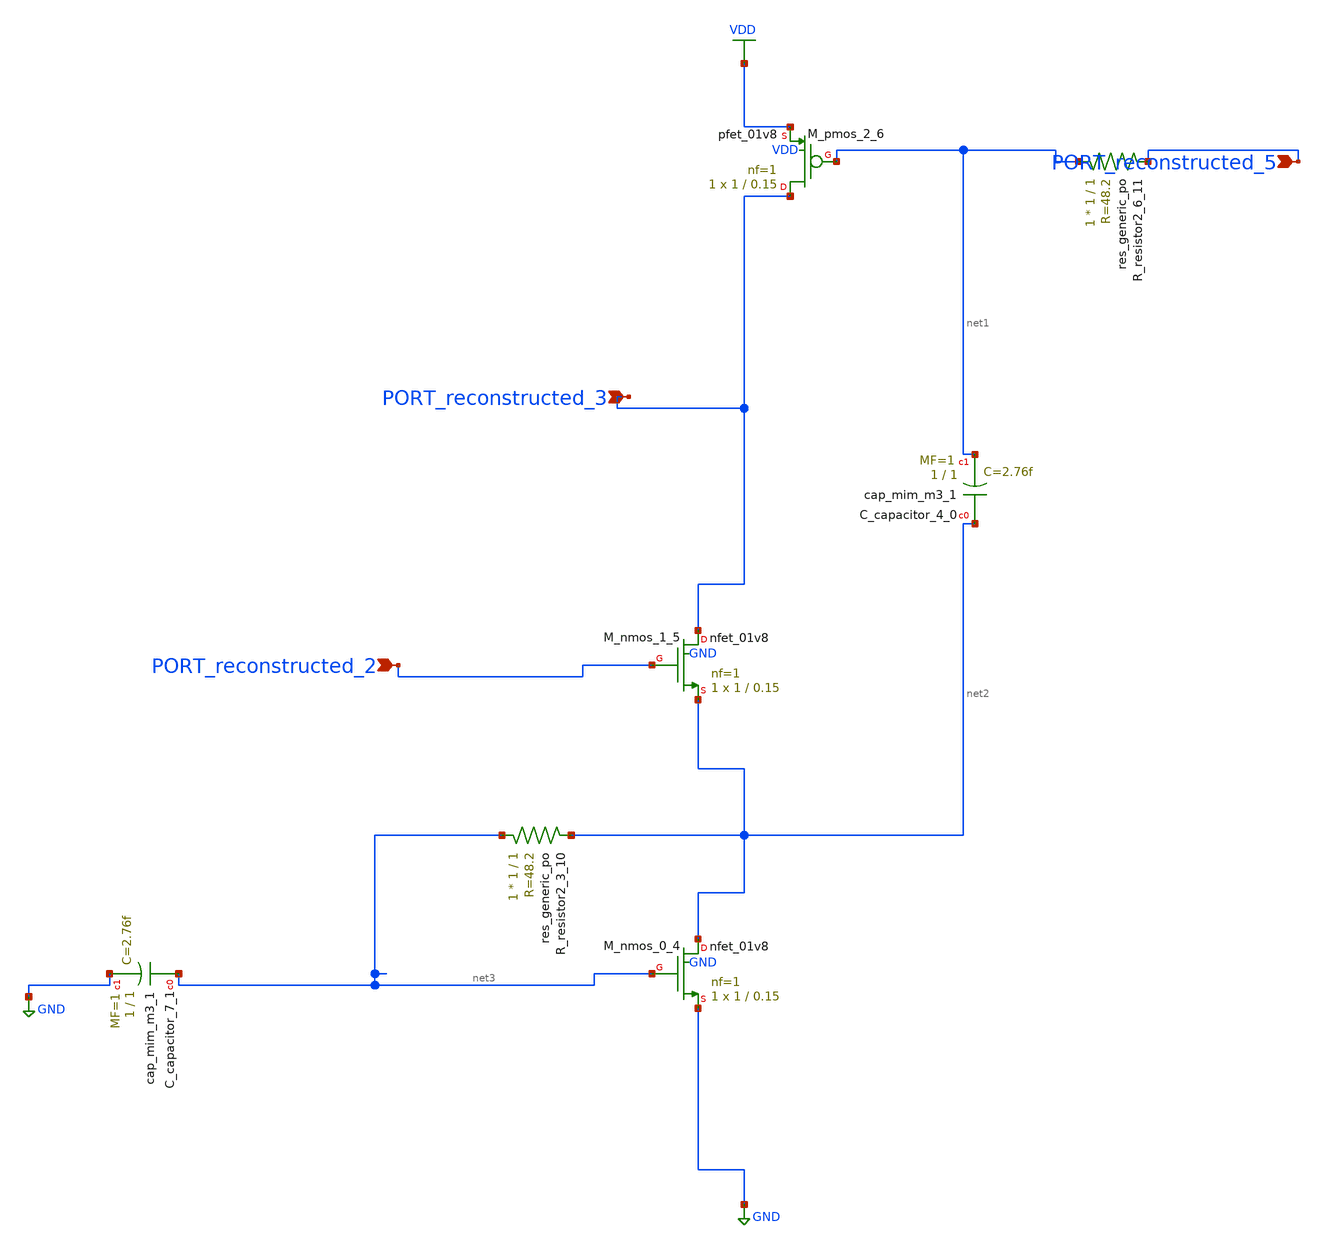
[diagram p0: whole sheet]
** sch_path: schematics/AMSNet/420.sch
**.subckt 420 PORT_reconstructed_3 PORT_reconstructed_2 PORT_reconstructed_5
*.ipin PORT_reconstructed_3
*.ipin PORT_reconstructed_2
*.ipin PORT_reconstructed_5
XC_capacitor_4_0 net2 net1 sky130_fd_pr__cap_mim_m3_1 W=1 L=1 MF=1 m=1
XC_capacitor_7_1 net3 GND sky130_fd_pr__cap_mim_m3_1 W=1 L=1 MF=1 m=1
XM_nmos_0_4 net2 net3 GND GND sky130_fd_pr__nfet_01v8 L=0.15 W=1 nf=1 ad='int((1 + 1)/2) * 1 / 1 * 0.29'
+ as='int((1 + 2)/2) * 1 / 1 * 0.29' pd='2*int((1 + 1)/2) * (1 / 1 + 0.29)' ps='2*int((1 + 2)/2) * (1 / 1 + 0.29)'
+ nrd='0.29 / 1 ' nrs='0.29 / 1 ' sa=0 sb=0 sd=0 mult=1 m=1
XM_nmos_1_5 PORT_reconstructed_3 PORT_reconstructed_2 net2 GND sky130_fd_pr__nfet_01v8 L=0.15 W=1 nf=1
+ ad='int((1 + 1)/2) * 1 / 1 * 0.29' as='int((1 + 2)/2) * 1 / 1 * 0.29' pd='2*int((1 + 1)/2) * (1 / 1 + 0.29)'
+ ps='2*int((1 + 2)/2) * (1 / 1 + 0.29)' nrd='0.29 / 1 ' nrs='0.29 / 1 ' sa=0 sb=0 sd=0 mult=1 m=1
XM_pmos_2_6 PORT_reconstructed_3 net1 VDD VDD sky130_fd_pr__pfet_01v8 L=0.15 W=1 nf=1 ad='int((1 + 1)/2) * 1 / 1 * 0.29'
+ as='int((1 + 2)/2) * 1 / 1 * 0.29' pd='2*int((1 + 1)/2) * (1 / 1 + 0.29)' ps='2*int((1 + 2)/2) * (1 / 1 + 0.29)'
+ nrd='0.29 / 1 ' nrs='0.29 / 1 ' sa=0 sb=0 sd=0 mult=1 m=1
XR_resistor2_3_10 net3 net2 sky130_fd_pr__res_generic_po W=1 L=1 m=1
XR_resistor2_6_11 net1 PORT_reconstructed_5 sky130_fd_pr__res_generic_po W=1 L=1 m=1
**.ends
.GLOBAL GND
.GLOBAL VDD
.end
